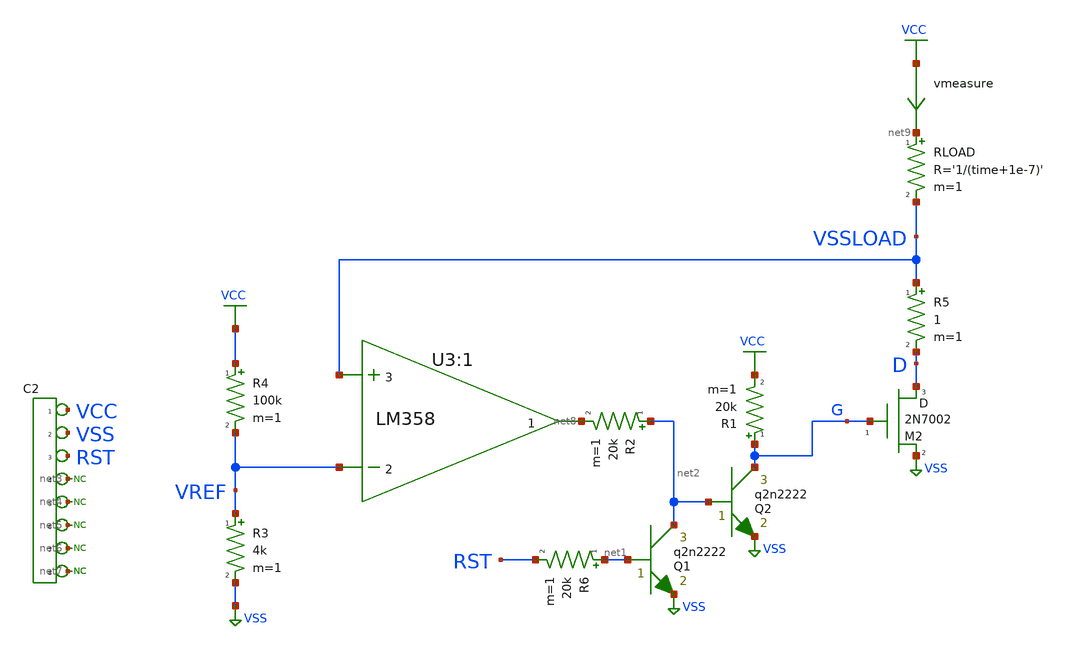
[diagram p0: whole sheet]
** sch_path: xschem_library/pcb/pcb_current_protection.sch
**.subckt pcb_current_protection
*connector(8,1) ?1 VCC ?1 VSS ?1 RST ?1 net3 ?1 net4 ?1 net5 ?1 net6 ?1 net7
* noconn #net7
* noconn #net7
* noconn #net6
XU3:1 VSSLOAD VREF VCC VSS net8 LM358
R3 VREF VSS 4k m=1
R4 VCC VREF 100k m=1
XM2 D G VSS M2N7002 m=1
R5 VSSLOAD D 1 m=1
* noconn #net5
* noconn #net4
* noconn #net3
RLOAD net9 VSSLOAD R='1/(time+1e-7)' m=1
vmeasure VCC net9 0
.save i(vmeasure)
R2 net2 net8 20k m=1
Q1 net2 net1 VSS q2n2222 area=1 m=1
R6 net1 RST 20k m=1
Q2 G net2 VSS q2n2222 area=1 m=1
R1 G VCC 20k m=1
**** begin user architecture code


*.option PARHIER=LOCAL RUNLVL=5 post MODMONTE=1 warn maxwarns=400 ingold=1


vvcc vcc 0 dc 5
vvss vss 0 dc 0
vrst rst 0 pwl 0 5 100u 5 101u 0

** models are generally not free: you must download
** SPICE models for active devices and put them  into the below
** referenced file in netlist/simulation directory.
.include "models_pcb_current_protection.txt"
* .dc RLOAD 10K 1 -0.001
.tran 10u 200m
.save all


**** end user architecture code
**.ends
.GLOBAL VSS
.GLOBAL VCC
.end
